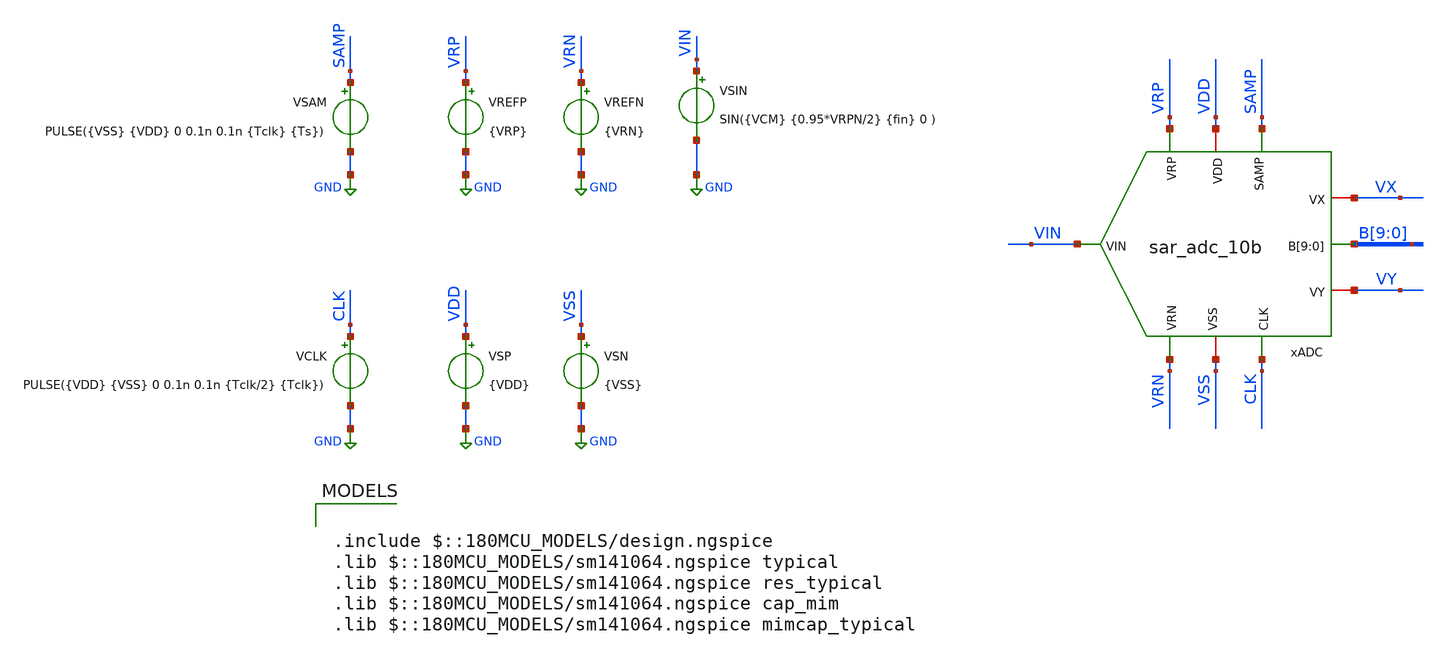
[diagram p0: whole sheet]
** sch_path: designs/sar_adc/top/sar_adc_10b/xschem/tb_sar_adc_10b.sch
**.subckt tb_sar_adc_10b
xADC VIN VDD VSS VRP VX B[9] B[8] B[7] B[6] B[5] B[4] B[3] B[2] B[1] B[0] SAMP CLK VY VRN
+ sar_adc_10b
VSP VDD GND {VDD}
VSN VSS GND {VSS}
VREFP VRP GND {VRP}
VREFN VRN GND {VRN}
VSIN VIN GND SIN({VCM} {0.95*VRPN/2} {fin} 0 )
VSAM SAMP GND PULSE({VSS} {VDD} 0 0.1n 0.1n {Tclk} {Ts})
VCLK CLK GND PULSE({VDD} {VSS} 0 0.1n 0.1n {Tclk/2} {Tclk})
**** begin user architecture code


.temp 27

* Voltages
.param VDD = 3.3
.param VSS = 0
.param VRP = 2.1
.param VRN = 1.2
.param VRPN = VRP-VRN
.param VCM = (VRP+VRN)/2

* Input parameters
.param Fs = 5Meg
.param Ns = 64
.param Nc = 7
.param fin = Nc/Ns*Fs

* Sampling clock
.param Ts = 1/Fs
.param Tclk = 1/(Fs*12)

.param sw_stat_global = 0
.param sw_stat_mismatch = 0

.control

* Local variables for .control
let Fs = 5Meg
let Ns = 1
let Nspare = 5

let tstep = 1/(Fs*12*100)
let tstop = (Ns + Nspare)/Fs

* Save main signals
save V(VIN) V(VX) V(VY) "B[9]" "B[8]" "B[7]" "B[6]" "B[5]" "B[4]" "B[3]" "B[2]" "B[1]" "B[0]"

* Transient simulation
tran $&tstep $&tstop

* Output waveforms
linearize
let vxy = V(VX)-V(VY)
let dout = ("B[9]"*1/2 + "B[8]"*1/4 + "B[7]"*1/8 + "B[6]"*1/16 + "B[5]"*1/32 + "B[4]"*1/64 +
+ "B[3]"*1/128 + "B[2]"*1/256 + "B[1]"*1/512 + "B[0]"*1/1024)

* export waveforms
wrdata tb_sar_adc_10b.csv v(VIN) v(VX) v(VY) dout

 * Plots
*plot V(VX) V(VY)
*plot V(VIN) V(VRP) V(VRN)
*plot V(CLK) V(SAMP)
*plot V(xADC.COMP)
plot vxy
plot dout

.endc



.include $::180MCU_MODELS/design.ngspice
.lib $::180MCU_MODELS/sm141064.ngspice typical
.lib $::180MCU_MODELS/sm141064.ngspice res_typical
.lib $::180MCU_MODELS/sm141064.ngspice cap_mim
.lib $::180MCU_MODELS/sm141064.ngspice mimcap_typical


**** end user architecture code
**.ends
.GLOBAL GND
.end
